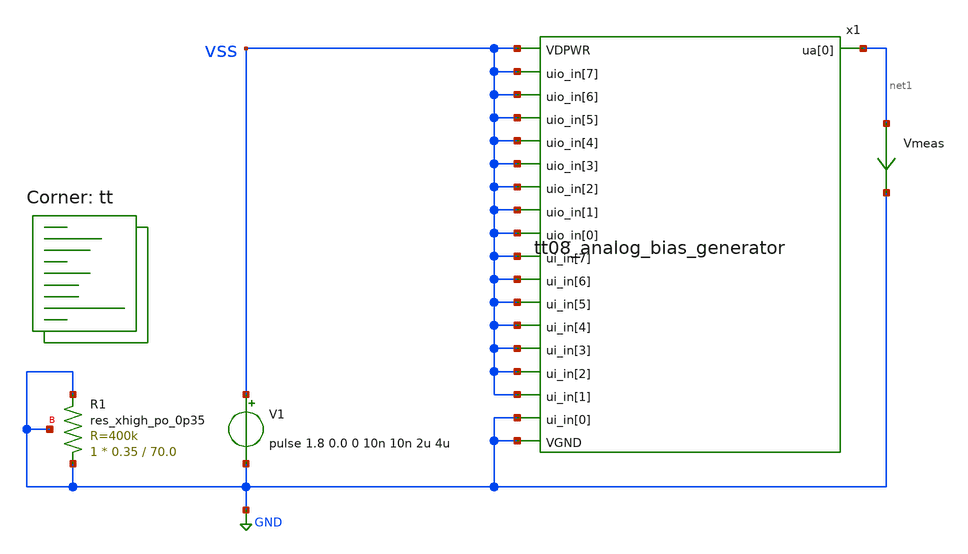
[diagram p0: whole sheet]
** sch_path: xschem/tb_tt08_analog_bias_generator.sch
**.subckt tb_tt08_analog_bias_generator
x1 vss net1 vss vss vss vss vss vss vss vss vss vss vss vss vss vss vss GND GND
+ tt08_analog_bias_generator
V1 vss GND pulse 1.8 0.0 0 10n 10n 2u 4u
XR1 GND GND GND sky130_fd_pr__res_xhigh_po_0p35 L=70.0 mult=1 m=1
Vmeas net1 GND 0
.save i(vmeas)
**** begin user architecture code
.lib $::SKYWATER_MODELS/sky130.lib.spice tt


.control
.option savecurrents
*.options temp=-40
dc V1 1.65 1.95 0.05 temp -40 125 15
plot i(Vmeas) title vs_Supply_tt_-40degto125deg
*plot v(ptat)
*plot v(drive)
dc temp -40 125 5
plot i(Vmeas) title vs_Temp_tt
*plot v(x1.drive) v(x1.ncascode)/2.0 title vs_Temp_tt
*plot v(x1.ptat) title vs_Temp_tt
set temp=-40
tran 2n 4u
*plot v(VSS) title Start_Up_tt_-40deg
plot i(Vmeas) title Start_Up_tt_-40deg
set temp=125
tran 2n 4u
*plot V(VSS) title Start_Up_tt_125deg
plot i(Vmeas) title Start_Up_tt_125deg
save all
set temp=27
op
*print all
write tb_tt08_analog_bias_generator.raw
.endc
.save all


**** end user architecture code
**.ends
.GLOBAL GND
.end
